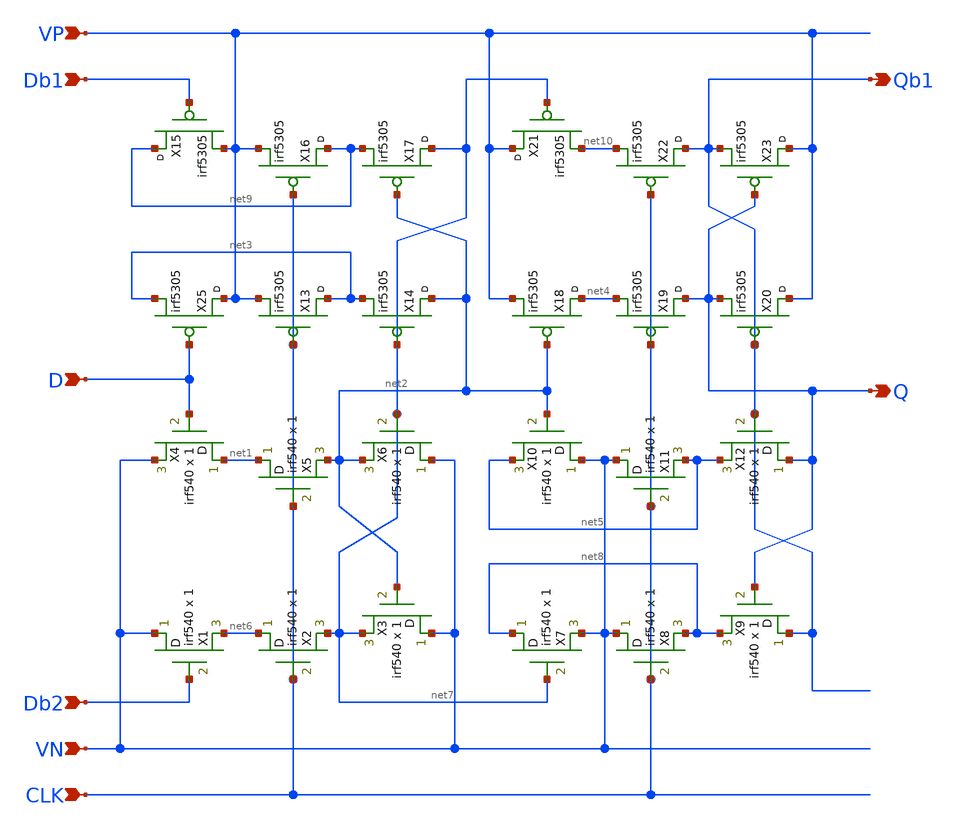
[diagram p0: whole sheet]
** sch_path: projects/negdff/xschem_ngspice/negdff.sch
**.subckt negdff D Db1 Db2 Q Qb1 CLK VP VN
*.ipin D
*.ipin Db1
*.ipin Db2
*.opin Q
*.opin Qb1
*.ipin CLK
*.ipin VP
*.ipin VN
X1 VN Db2 net6 irf540 m=1
X2 net6 CLK net7 irf540 m=1
X3 VN net2 net7 irf540 m=1
X4 net1 D VN irf540 m=1
X5 net1 CLK net2 irf540 m=1
X6 VN net7 net2 irf540 m=1
X7 net8 net7 VN irf540 m=1
X8 VN CLK net8 irf540 m=1
X9 Qb1 Q net8 irf540 m=1
X10 VN net2 net5 irf540 m=1
X11 VN CLK net5 irf540 m=1
X12 Q Qb1 net5 irf540 m=1
X25 VP D net3 irf5305
X13 net3 CLK VP irf5305
X14 net2 net7 net3 irf5305
X15 net9 Db1 VP irf5305
X16 net9 CLK VP irf5305
X17 net7 net2 net9 irf5305
X18 net4 net2 VP irf5305
X19 Q CLK net4 irf5305
X20 VP Qb1 Q irf5305
X21 VP net7 net10 irf5305
X22 Qb1 CLK net10 irf5305
X23 VP Q Qb1 irf5305
**.ends
.end
